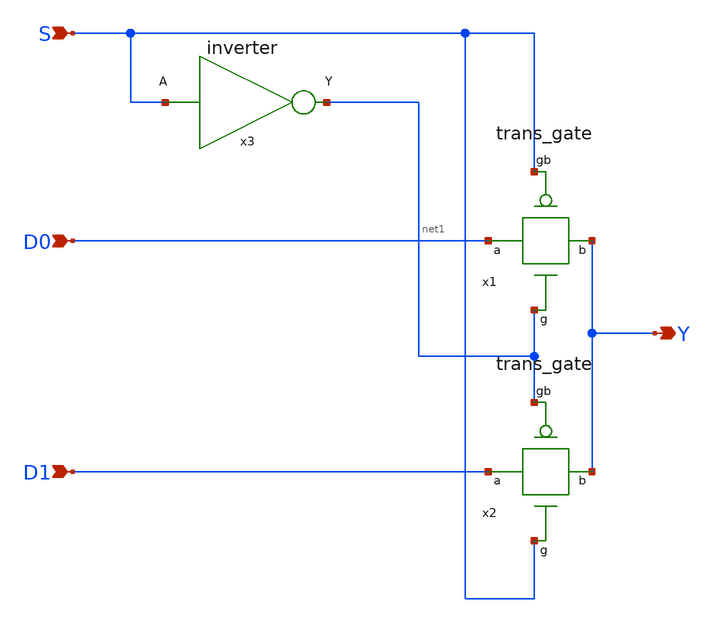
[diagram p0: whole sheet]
** sch_path: mux2_1.sch
**.subckt mux2_1 S D0 D1 Y
*.ipin S
*.ipin D0
*.ipin D1
*.opin Y
x1 S D0 Y net1 trans_gate
x2 net1 D1 Y S trans_gate
x3 net1 S inverter
**.ends

* expanding   symbol:  trans_gate.sym # of pins=4
** sym_path: trans_gate.sym
** sch_path: trans_gate.sch
.subckt trans_gate gb a b g
*.ipin gb
*.ipin a
*.ipin g
*.opin b
XM1 a g b GND sky130_fd_pr__nfet_01v8 L=0.15 W=1 nf=1 ad='int((nf+1)/2) * W/nf * 0.29' as='int((nf+2)/2) * W/nf * 0.29'
+ pd='2*int((nf+1)/2) * (W/nf + 0.29)' ps='2*int((nf+2)/2) * (W/nf + 0.29)' nrd='0.29 / W' nrs='0.29 / W'
+ sa=0 sb=0 sd=0 mult=1 m=1
XM2 a gb b VDD sky130_fd_pr__pfet_01v8 L=0.15 W=1 nf=1 ad='int((nf+1)/2) * W/nf * 0.29' as='int((nf+2)/2) * W/nf * 0.29'
+ pd='2*int((nf+1)/2) * (W/nf + 0.29)' ps='2*int((nf+2)/2) * (W/nf + 0.29)' nrd='0.29 / W' nrs='0.29 / W'
+ sa=0 sb=0 sd=0 mult=1 m=1
.ends


* expanding   symbol:  inverter.sym # of pins=2
** sym_path: inverter.sym
** sch_path: inverter.sch
.subckt inverter Y A
*.ipin A
*.opin Y
XM1 Y A GND GND sky130_fd_pr__nfet_01v8 L=0.15 W=1 nf=1 ad='int((nf+1)/2) * W/nf * 0.29' as='int((nf+2)/2) * W/nf * 0.29'
+ pd='2*int((nf+1)/2) * (W/nf + 0.29)' ps='2*int((nf+2)/2) * (W/nf + 0.29)' nrd='0.29 / W' nrs='0.29 / W'
+ sa=0 sb=0 sd=0 mult=1 m=1
XM2 Y A VDD VDD sky130_fd_pr__pfet_01v8 L=0.15 W=1 nf=1 ad='int((nf+1)/2) * W/nf * 0.29' as='int((nf+2)/2) * W/nf * 0.29'
+ pd='2*int((nf+1)/2) * (W/nf + 0.29)' ps='2*int((nf+2)/2) * (W/nf + 0.29)' nrd='0.29 / W' nrs='0.29 / W'
+ sa=0 sb=0 sd=0 mult=1 m=1
.ends

.GLOBAL VDD
.GLOBAL GND
.end
